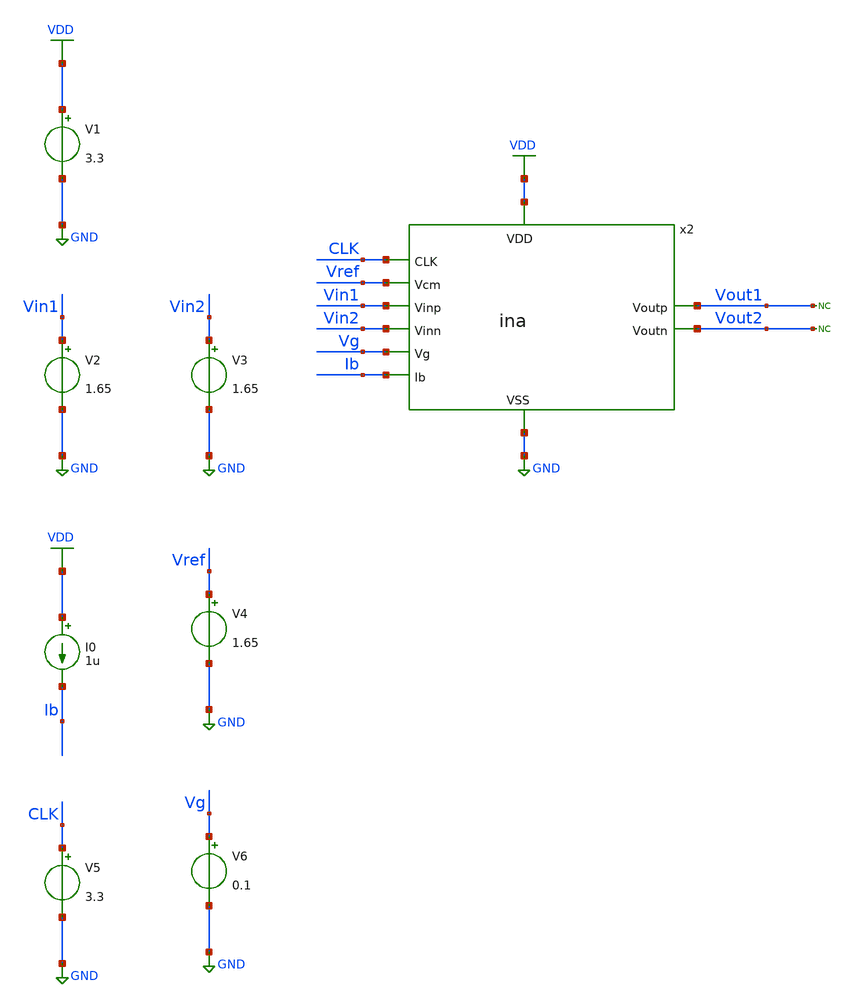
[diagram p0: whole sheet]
** sch_path: designs/libs/tb_ina/tb_ina_stb/tb_ina_stb.sch
**.subckt tb_ina_stb
V1 VDD GND 3.3
V2 Vin1 GND 1.65
V3 Vin2 GND 1.65
I0 VDD Ib 1u
V4 Vref GND 1.65
x2 Vg VDD Vin1 Vin2 CLK Vout1 Vout2 GND Vref Ib ina
V5 CLK GND 3.3
V6 Vg GND 0.1
* noconn Vout1
* noconn Vout2
**** begin user architecture code

.include $::180MCU_MODELS/design.ngspice
.lib $::180MCU_MODELS/sm141064.ngspice typical
.lib $::180MCU_MODELS/sm141064.ngspice cap_mim
.lib $::180MCU_MODELS/sm141064.ngspice moscap_typical
.lib $::180MCU_MODELS/sm141064.ngspice mimcap_typical
.lib $::180MCU_MODELS/sm141064.ngspice res_typical
* .lib $::180MCU_MODELS/sm141064.ngspice res_statistical
* ngspice commands




.control
save all

run
set color0 = white

*************************************
** PARAMETERS
*************************************

let Vdd  = 3.3
let Vcm  = 1.65
let Ibias = 2u
let Vg  = 0.1

*************************************
** CHOPPER PARAMETERS
*************************************

let fchop = 4k
let tper = 1/fchop
let ton = tper/2
let tr = 10n
let tf = 10n

*************************************
** SOURCES
*************************************

alter @V1[DC] = $&Vdd
alter @V2[DC] = $&Vcm
alter @V3[DC] = $&Vcm
alter @V2[ACMAG] = 0.5
alter @V3[ACMAG] = -0.5
alter @V4[DC] = $&Vcm
alter @I0[DC] = $&Ibias
alter @V5[PULSE] = [ 0 $&Vdd 0 $&tr $&tf $&ton $&tper 0 ]
alter @V6[DC] = $&Vg

*************************************
** AC SIMULATION
*************************************

ac dec 100 0.01 1G

*************************************
** MEASUREMENTS
*************************************

let vout_diff = v(Vout1)-v(Vout2)
let vin_diff  = v(Vin1)-v(Vin2)
let Av = vout_diff/vin_diff
let gain_db = db(Av)
let phase_deg = cph(Av)*180/pi
meas ac UGF WHEN gain_db=0
meas ac phase_UGF FIND phase_deg WHEN gain_db=0
let PM = phase_UGF + 180
print PM

*************************************
** PLOTS
*************************************

setplot ac1
plot phase_deg

*************************************
** SAVE
*************************************

write tb_ina_stb.raw

.endc
* ngspice commands



**** end user architecture code
**.ends
.GLOBAL GND
.GLOBAL VDD
.end
